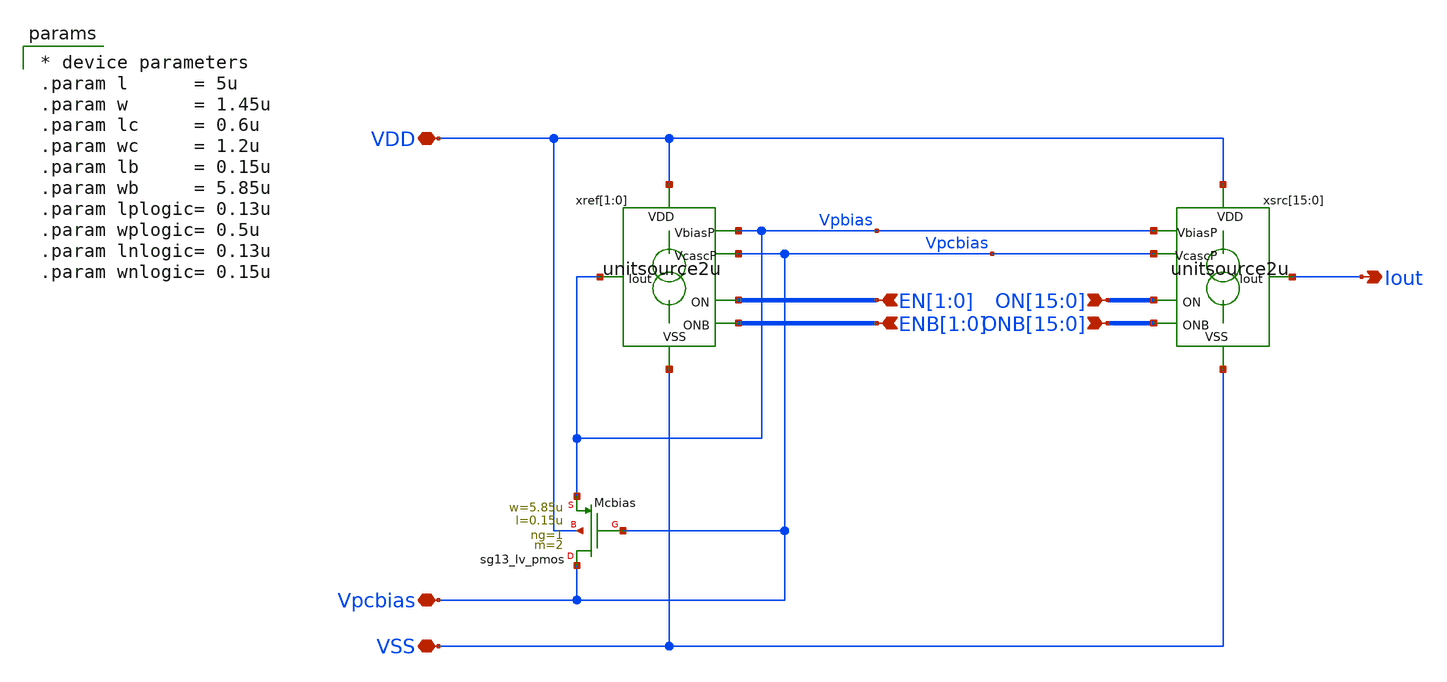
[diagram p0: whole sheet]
** sch_path: xschem/dac2u16out2in.sch
**.subckt dac2u16out2in Iout
*+ ON[15],ON[14],ON[13],ON[12],ON[11],ON[10],ON[9],ON[8],ON[7],ON[6],ON[5],ON[4],ON[3],ON[2],ON[1],ON[0]
*+ ONB[15],ONB[14],ONB[13],ONB[12],ONB[11],ONB[10],ONB[9],ONB[8],ONB[7],ONB[6],ONB[5],ONB[4],ONB[3],ONB[2],ONB[1],ONB[0] VSS VDD Vpcbias EN[1],EN[0] ENB[1],ENB[0]
*.opin Iout
*.ipin
*+ ON[15],ON[14],ON[13],ON[12],ON[11],ON[10],ON[9],ON[8],ON[7],ON[6],ON[5],ON[4],ON[3],ON[2],ON[1],ON[0]
*.ipin
*+ ONB[15],ONB[14],ONB[13],ONB[12],ONB[11],ONB[10],ONB[9],ONB[8],ONB[7],ONB[6],ONB[5],ONB[4],ONB[3],ONB[2],ONB[1],ONB[0]
*.iopin VSS
*.iopin VDD
*.iopin Vpcbias
*.ipin EN[1],EN[0]
*.ipin ENB[1],ENB[0]
XMcbias Vpcbias Vpcbias Vpbias VDD sg13_lv_pmos w=5.85u l=0.15u ng=1 m=2 mm_ok=1
xref[1] VDD Vpbias EN[1] ENB[1] Vpbias Vpcbias VSS unitsource2u
xref[0] VDD Vpbias EN[0] ENB[0] Vpbias Vpcbias VSS unitsource2u
xsrc[15] VDD Vpbias ON[15] ONB[15] Iout Vpcbias VSS unitsource2u
xsrc[14] VDD Vpbias ON[14] ONB[14] Iout Vpcbias VSS unitsource2u
xsrc[13] VDD Vpbias ON[13] ONB[13] Iout Vpcbias VSS unitsource2u
xsrc[12] VDD Vpbias ON[12] ONB[12] Iout Vpcbias VSS unitsource2u
xsrc[11] VDD Vpbias ON[11] ONB[11] Iout Vpcbias VSS unitsource2u
xsrc[10] VDD Vpbias ON[10] ONB[10] Iout Vpcbias VSS unitsource2u
xsrc[9] VDD Vpbias ON[9] ONB[9] Iout Vpcbias VSS unitsource2u
xsrc[8] VDD Vpbias ON[8] ONB[8] Iout Vpcbias VSS unitsource2u
xsrc[7] VDD Vpbias ON[7] ONB[7] Iout Vpcbias VSS unitsource2u
xsrc[6] VDD Vpbias ON[6] ONB[6] Iout Vpcbias VSS unitsource2u
xsrc[5] VDD Vpbias ON[5] ONB[5] Iout Vpcbias VSS unitsource2u
xsrc[4] VDD Vpbias ON[4] ONB[4] Iout Vpcbias VSS unitsource2u
xsrc[3] VDD Vpbias ON[3] ONB[3] Iout Vpcbias VSS unitsource2u
xsrc[2] VDD Vpbias ON[2] ONB[2] Iout Vpcbias VSS unitsource2u
xsrc[1] VDD Vpbias ON[1] ONB[1] Iout Vpcbias VSS unitsource2u
xsrc[0] VDD Vpbias ON[0] ONB[0] Iout Vpcbias VSS unitsource2u
**** begin user architecture code

* device parameters
.param l      = 5u
.param w      = 1.45u
.param lc     = 0.6u
.param wc     = 1.2u
.param lb     = 0.15u
.param wb     = 5.85u
.param lplogic= 0.13u
.param wplogic= 0.5u
.param lnlogic= 0.13u
.param wnlogic= 0.15u


**** end user architecture code
**.ends

* expanding   symbol:  unitsource2u.sym # of pins=7
** sym_path: xschem/unitsource2u.sym
** sch_path: xschem/unitsource2u.sch
.subckt unitsource2u VDD VbiasP ON ONB Iout VcascP VSS
*.iopin VSS
*.iopin VDD
*.iopin VbiasP
*.iopin VcascP
*.ipin ON
*.ipin ONB
*.iopin Iout
xnonoverlap VDD VSS ON ONB on_n off_n nonoverlap
xsw VDD off_n Vcasc on_n VcascP cascodeswitch_pmos
xsrc VDD VbiasP Vcasc Iout pcsource2u
.ends


* expanding   symbol:  nonoverlap.sym # of pins=6
** sym_path: xschem/nonoverlap.sym
** sch_path: xschem/nonoverlap.sch
.subckt nonoverlap VDD VSS INP INN OUTN OUTP
*.iopin VSS
*.iopin VDD
*.ipin INP
*.ipin INN
*.opin OUTP
*.opin OUTN
XM1 OUTN INP VDD VDD sg13_lv_pmos w=0.3u l=0.13u ng=1 m=1 mm_ok=1
XM2 OUTP INN VDD VDD sg13_lv_pmos w=0.3u l=0.13u ng=1 m=1 mm_ok=1
XM3 OUTN OUTP VSS VSS sg13_lv_nmos w=0.15u l=0.52u ng=1 m=1 mm_ok=1
XM4 OUTP OUTN VSS VSS sg13_lv_nmos w=0.15u l=0.52u ng=1 m=1 mm_ok=1
.ends


* expanding   symbol:  cascodeswitch_pmos.sym # of pins=5
** sym_path: xschem/cascodeswitch_pmos.sym
** sch_path: xschem/cascodeswitch_pmos.sch
.subckt cascodeswitch_pmos VDD off_n Vcasc on_n Vbpcasc
*.ipin off_n
*.ipin Vbpcasc
*.opin Vcasc
*.ipin on_n
*.ipin VDD
XMpullup Vcasc off_n VDD VDD sg13_lv_pmos w=0.3u l=0.13u ng=1 m=1 mm_ok=1
XMbias Vbpcasc on_n Vcasc VDD sg13_lv_pmos w=0.3u l=0.13u ng=1 m=1 mm_ok=1
.ends


* expanding   symbol:  pcsource2u.sym # of pins=4
** sym_path: xschem/pcsource2u.sym
** sch_path: xschem/pcsource2u.sch
.subckt pcsource2u VDD VbiasP VcascodeP Iout
*.ipin VcascodeP
*.ipin VbiasP
*.opin Iout
*.ipin VDD
XMsrc drain net4 VDD net1 sg13_lv_pmos w=1.45u l=5u ng=1 m=1 mm_ok=1
XMcasc Iout net3 drain net2 sg13_lv_pmos w=1.2u l=0.6u ng=1 m=1 mm_ok=1
Vgsrc net4 VbiasP 0
.save i(vgsrc)
Vgcasc net3 VcascodeP 0
.save i(vgcasc)
Vbsrc VDD net1 0
.save i(vbsrc)
Vbcasc VDD net2 0
.save i(vbcasc)
.ends

.end
